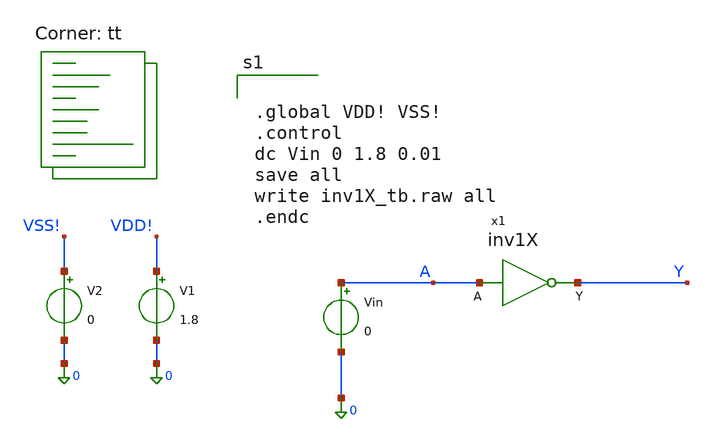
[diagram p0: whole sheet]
** sch_path: inv1X/inv1X_tb.sch
**.subckt inv1X_tb
V1 VDD! 0 1.8
Vin A 0 0
V2 VSS! 0 0
x1 Y A inv1X
**** begin user architecture code
.lib $::SKYWATER_MODELS/sky130.lib.spice tt


.global VDD! VSS!
.control
dc Vin 0 1.8 0.01
save all
write inv1X_tb.raw all
.endc


**** end user architecture code
**.ends

* expanding   symbol:  /foss/designs/micron/micron_stdcells/inv1X/inv1X.sym # of pins=2
** sym_path: inv1X/inv1X.sym
** sch_path: inv1X/inv1X.sch
.subckt inv1X Y A
*.ipin A
*.opin Y
XM1 Y A VSS! VSS! sky130_fd_pr__nfet_01v8 L=0.15 W=0.42 nf=1 ad='int((1 + 1)/2) * 0.42 / 1 * 0.29' as='int((1 + 2)/2) * 0.42 / 1 * 0.29'
+ pd='2*int((1 + 1)/2) * (0.42 / 1 + 0.29)' ps='2*int((1 + 2)/2) * (0.42 / 1 + 0.29)' nrd='0.29 / 0.42 '
+ nrs='0.29 / 0.42 ' sa=0 sb=0 sd=0 mult=1 m=1
XM2 Y A VDD! VDD! sky130_fd_pr__pfet_01v8 L=0.15 W=0.84 nf=1 ad='int((1 + 1)/2) * 0.84 / 1 * 0.29' as='int((1 + 2)/2) * 0.84 / 1 * 0.29'
+ pd='2*int((1 + 1)/2) * (0.84 / 1 + 0.29)' ps='2*int((1 + 2)/2) * (0.84 / 1 + 0.29)' nrd='0.29 / 0.84 '
+ nrs='0.29 / 0.84 ' sa=0 sb=0 sd=0 mult=1 m=1
.ends

.end
